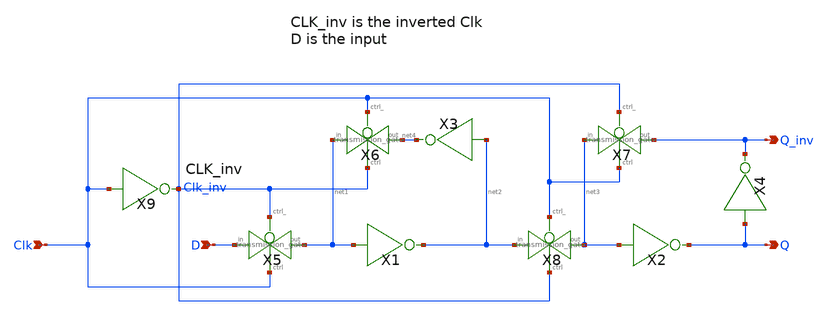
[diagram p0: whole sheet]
** sch_path: xschem/D_flip_flop/d_flip_flop.sch
**.subckt d_flip_flop D Clk Q_inv Q
*.ipin D
*.ipin Clk
*.opin Q_inv
*.opin Q
X1 net1 net2 inv
X2 net3 Q inv
X3 net2 net4 inv
X4 Q Q_inv inv
X5 D net1 Clk_inv Clk transmission_gate
X6 net1 net4 Clk Clk_inv transmission_gate
X7 net3 Q_inv Clk_inv Clk transmission_gate
X8 net2 net3 Clk Clk_inv transmission_gate
X9 Clk Clk_inv inv
**.ends

* expanding   symbol:  inv/inv.sym # of pins=2
** sym_path: xschem/inv/inv.sym
** sch_path: xschem/inv/inv.sch
.subckt inv in out
*.ipin in
*.iopin out
XM1 out in GND GND sky130_fd_pr__nfet_01v8 L=0.18 W=0.5 nf=1 ad='int((nf+1)/2) * W/nf * 0.29' as='int((nf+2)/2) * W/nf * 0.29'
+ pd='2*int((nf+1)/2) * (W/nf + 0.29)' ps='2*int((nf+2)/2) * (W/nf + 0.29)' nrd='0.29 / W' nrs='0.29 / W'
+ sa=0 sb=0 sd=0 mult=1 m=1
XM2 out in VDD VDD sky130_fd_pr__pfet_01v8 L=0.18 W=1 nf=1 ad='int((nf+1)/2) * W/nf * 0.29' as='int((nf+2)/2) * W/nf * 0.29'
+ pd='2*int((nf+1)/2) * (W/nf + 0.29)' ps='2*int((nf+2)/2) * (W/nf + 0.29)' nrd='0.29 / W' nrs='0.29 / W'
+ sa=0 sb=0 sd=0 mult=1 m=1
.ends


* expanding   symbol:  transmission_gate/transmission_gate.sym # of pins=4
** sym_path: xschem/transmission_gate/transmission_gate.sym
** sch_path: xschem/transmission_gate/transmission_gate.sch
.subckt transmission_gate in out ctrl_ ctrl
*.iopin in
*.iopin out
*.ipin ctrl_
*.ipin ctrl
XM3 in ctrl out GND sky130_fd_pr__nfet_01v8 L=0.18 W=1 nf=1 ad='int((nf+1)/2) * W/nf * 0.29' as='int((nf+2)/2) * W/nf * 0.29'
+ pd='2*int((nf+1)/2) * (W/nf + 0.29)' ps='2*int((nf+2)/2) * (W/nf + 0.29)' nrd='0.29 / W' nrs='0.29 / W'
+ sa=0 sb=0 sd=0 mult=1 m=1
XM4 out ctrl_ in VDD sky130_fd_pr__pfet_01v8 L=0.18 W=1 nf=1 ad='int((nf+1)/2) * W/nf * 0.29' as='int((nf+2)/2) * W/nf * 0.29'
+ pd='2*int((nf+1)/2) * (W/nf + 0.29)' ps='2*int((nf+2)/2) * (W/nf + 0.29)' nrd='0.29 / W' nrs='0.29 / W'
+ sa=0 sb=0 sd=0 mult=1 m=1
.ends

.GLOBAL VDD
.GLOBAL GND
.end
